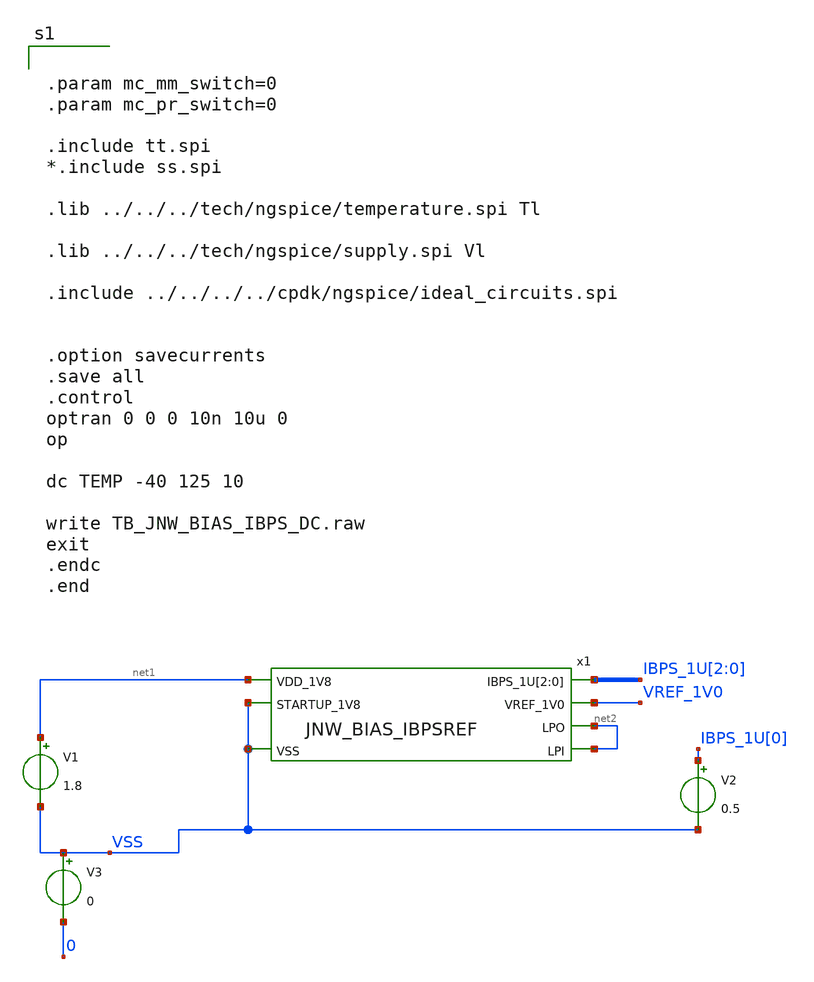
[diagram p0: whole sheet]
** sch_path: design/JNW_BIAS_SKY130A/TB_JNW_BIAS_IBPS_DC.sch
**.subckt TB_JNW_BIAS_IBPS_DC
V1 net1 VSS 1.8
V2 IBPS_1U[0] VSS 0.5
V3 VSS 0 0
x1 IBPS_1U[2] IBPS_1U[1] IBPS_1U[0] net1 net2 VSS VREF_1V0 net2 VSS JNW_BIAS_IBPSREF
**** begin user architecture code


.param mc_mm_switch=0
.param mc_pr_switch=0

.include tt.spi
*.include ss.spi

.lib ../../../tech/ngspice/temperature.spi Tl

.lib ../../../tech/ngspice/supply.spi Vl

.include ../../../../cpdk/ngspice/ideal_circuits.spi


.option savecurrents
.save all
.control
optran 0 0 0 10n 10u 0
op

dc TEMP -40 125 10

write TB_JNW_BIAS_IBPS_DC.raw
exit
.endc
.end



**** end user architecture code
**.ends
.end
